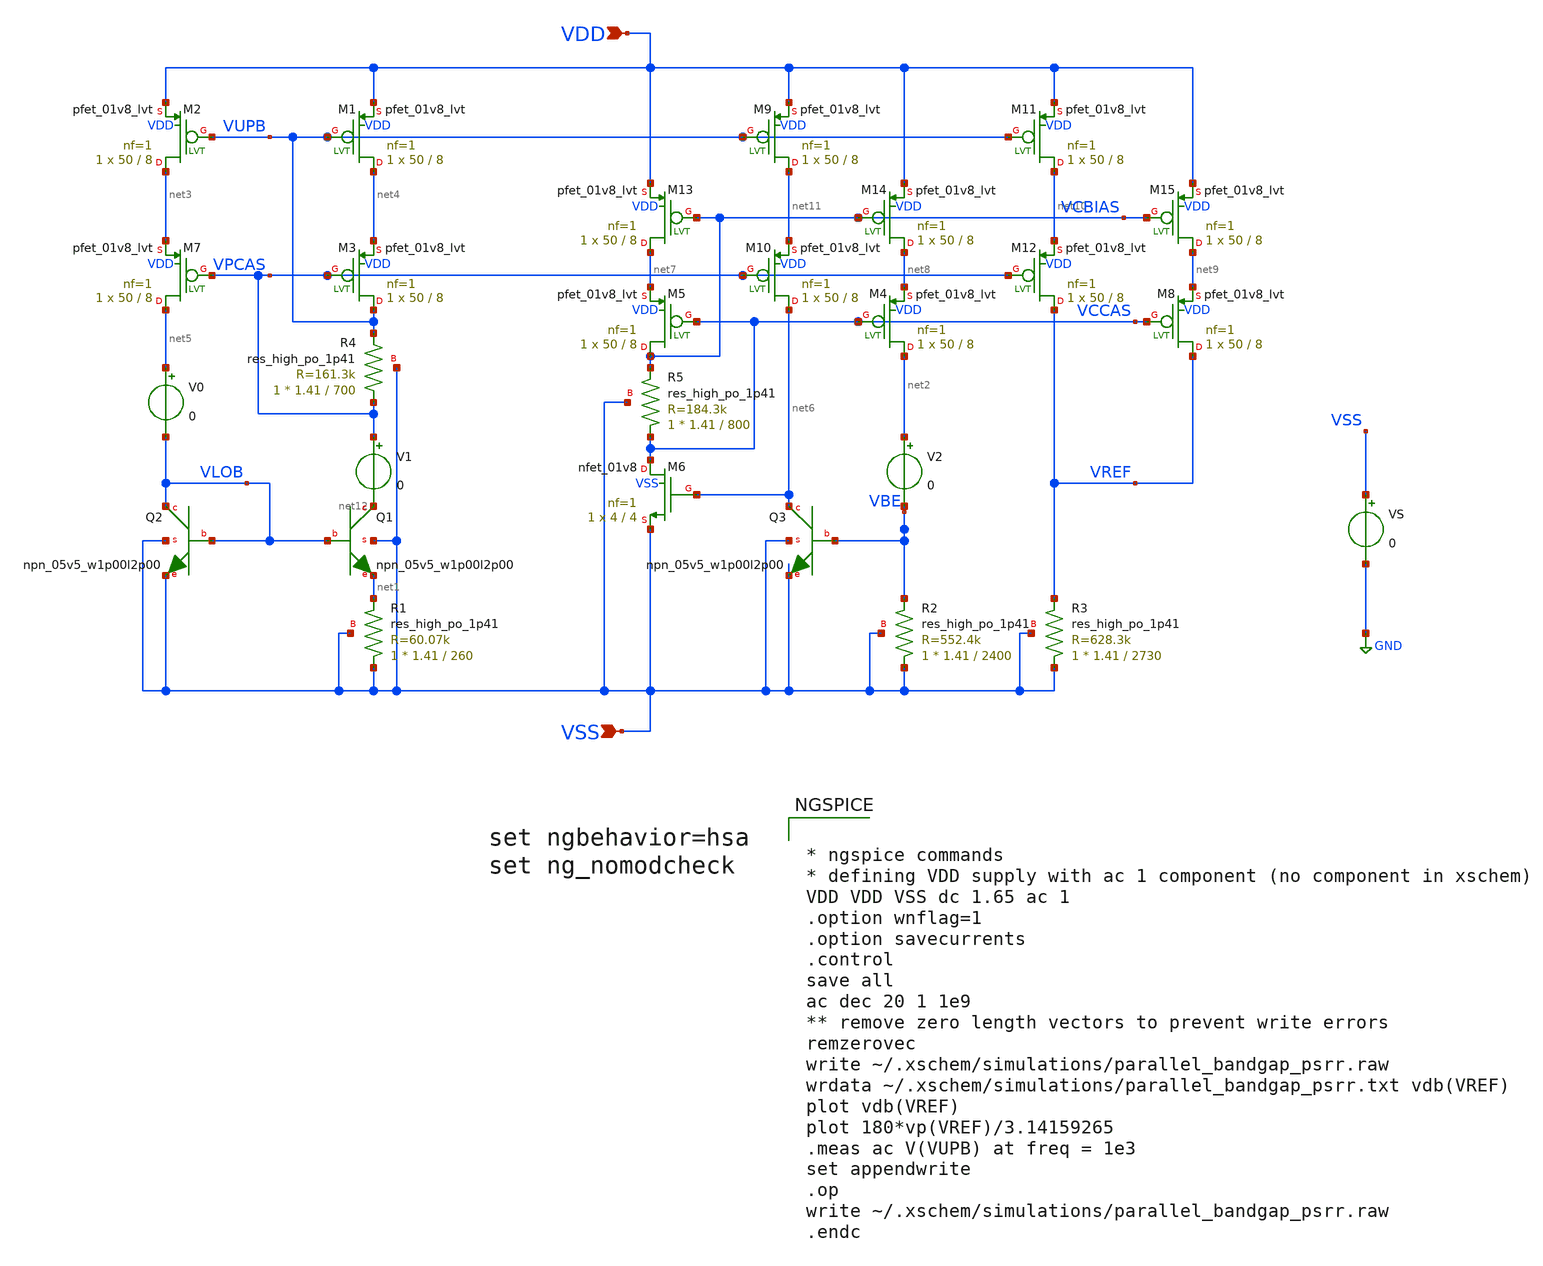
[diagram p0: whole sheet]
** sch_path: designs/parallel_bandgap_psrr.sch
**.subckt parallel_bandgap_psrr VDD VSS
*.ipin VDD
*.ipin VSS
XM1 net4 VUPB VDD VDD sky130_fd_pr__pfet_01v8_lvt L=8 W=50 nf=1 ad='int((nf+1)/2) * W/nf * 0.29' as='int((nf+2)/2) * W/nf * 0.29'
+ pd='2*int((nf+1)/2) * (W/nf + 0.29)' ps='2*int((nf+2)/2) * (W/nf + 0.29)' nrd='0.29 / W' nrs='0.29 / W'
+ sa=0 sb=0 sd=0 mult=1 m=1
XM2 net3 VUPB VDD VDD sky130_fd_pr__pfet_01v8_lvt L=8 W=50 nf=1 ad='int((nf+1)/2) * W/nf * 0.29' as='int((nf+2)/2) * W/nf * 0.29'
+ pd='2*int((nf+1)/2) * (W/nf + 0.29)' ps='2*int((nf+2)/2) * (W/nf + 0.29)' nrd='0.29 / W' nrs='0.29 / W'
+ sa=0 sb=0 sd=0 mult=1 m=1
XQ1 net12 VLOB net1 VSS sky130_fd_pr__npn_05v5_w1p00l2p00
XQ2 VLOB VLOB VSS VSS sky130_fd_pr__npn_05v5_w1p00l2p00
XR1 VSS net1 VSS sky130_fd_pr__res_high_po_1p41 L=260 mult=1 m=1
XQ3 net6 VBE VSS VSS sky130_fd_pr__npn_05v5_w1p00l2p00
XR2 VSS VBE VSS sky130_fd_pr__res_high_po_1p41 L=2400 mult=1 m=1
XM4 net2 VCCAS net8 VDD sky130_fd_pr__pfet_01v8_lvt L=8 W=50 nf=1 ad='int((nf+1)/2) * W/nf * 0.29' as='int((nf+2)/2) * W/nf * 0.29'
+ pd='2*int((nf+1)/2) * (W/nf + 0.29)' ps='2*int((nf+2)/2) * (W/nf + 0.29)' nrd='0.29 / W' nrs='0.29 / W'
+ sa=0 sb=0 sd=0 mult=1 m=1
XM5 VCBIAS VCCAS net7 VDD sky130_fd_pr__pfet_01v8_lvt L=8 W=50 nf=1 ad='int((nf+1)/2) * W/nf * 0.29'
+ as='int((nf+2)/2) * W/nf * 0.29' pd='2*int((nf+1)/2) * (W/nf + 0.29)' ps='2*int((nf+2)/2) * (W/nf + 0.29)'
+ nrd='0.29 / W' nrs='0.29 / W' sa=0 sb=0 sd=0 mult=1 m=1
XM6 VCCAS net6 VSS VSS sky130_fd_pr__nfet_01v8 L=4 W=4 nf=1 ad='int((nf+1)/2) * W/nf * 0.29' as='int((nf+2)/2) * W/nf * 0.29'
+ pd='2*int((nf+1)/2) * (W/nf + 0.29)' ps='2*int((nf+2)/2) * (W/nf + 0.29)' nrd='0.29 / W' nrs='0.29 / W'
+ sa=0 sb=0 sd=0 mult=1 m=1
XR3 VSS VREF VSS sky130_fd_pr__res_high_po_1p41 L=2730 mult=1 m=1
XM8 VREF VCCAS net9 VDD sky130_fd_pr__pfet_01v8_lvt L=8 W=50 nf=1 ad='int((nf+1)/2) * W/nf * 0.29' as='int((nf+2)/2) * W/nf * 0.29'
+ pd='2*int((nf+1)/2) * (W/nf + 0.29)' ps='2*int((nf+2)/2) * (W/nf + 0.29)' nrd='0.29 / W' nrs='0.29 / W'
+ sa=0 sb=0 sd=0 mult=1 m=1
V0 net5 VLOB 0
.save i(v0)
V2 net2 VBE 0
.save i(v2)
V1 VPCAS net12 0
.save i(v1)
XM3 VUPB VPCAS net4 VDD sky130_fd_pr__pfet_01v8_lvt L=8 W=50 nf=1 ad='int((nf+1)/2) * W/nf * 0.29' as='int((nf+2)/2) * W/nf * 0.29'
+ pd='2*int((nf+1)/2) * (W/nf + 0.29)' ps='2*int((nf+2)/2) * (W/nf + 0.29)' nrd='0.29 / W' nrs='0.29 / W'
+ sa=0 sb=0 sd=0 mult=1 m=1
XM7 net5 VPCAS net3 VDD sky130_fd_pr__pfet_01v8_lvt L=8 W=50 nf=1 ad='int((nf+1)/2) * W/nf * 0.29' as='int((nf+2)/2) * W/nf * 0.29'
+ pd='2*int((nf+1)/2) * (W/nf + 0.29)' ps='2*int((nf+2)/2) * (W/nf + 0.29)' nrd='0.29 / W' nrs='0.29 / W'
+ sa=0 sb=0 sd=0 mult=1 m=1
XR4 VPCAS VUPB VSS sky130_fd_pr__res_high_po_1p41 L=700 mult=1 m=1
XM9 net11 VUPB VDD VDD sky130_fd_pr__pfet_01v8_lvt L=8 W=50 nf=1 ad='int((nf+1)/2) * W/nf * 0.29' as='int((nf+2)/2) * W/nf * 0.29'
+ pd='2*int((nf+1)/2) * (W/nf + 0.29)' ps='2*int((nf+2)/2) * (W/nf + 0.29)' nrd='0.29 / W' nrs='0.29 / W'
+ sa=0 sb=0 sd=0 mult=1 m=1
XM10 net6 VPCAS net11 VDD sky130_fd_pr__pfet_01v8_lvt L=8 W=50 nf=1 ad='int((nf+1)/2) * W/nf * 0.29'
+ as='int((nf+2)/2) * W/nf * 0.29' pd='2*int((nf+1)/2) * (W/nf + 0.29)' ps='2*int((nf+2)/2) * (W/nf + 0.29)'
+ nrd='0.29 / W' nrs='0.29 / W' sa=0 sb=0 sd=0 mult=1 m=1
XM11 net10 VUPB VDD VDD sky130_fd_pr__pfet_01v8_lvt L=8 W=50 nf=1 ad='int((nf+1)/2) * W/nf * 0.29' as='int((nf+2)/2) * W/nf * 0.29'
+ pd='2*int((nf+1)/2) * (W/nf + 0.29)' ps='2*int((nf+2)/2) * (W/nf + 0.29)' nrd='0.29 / W' nrs='0.29 / W'
+ sa=0 sb=0 sd=0 mult=1 m=1
XM12 VREF VPCAS net10 VDD sky130_fd_pr__pfet_01v8_lvt L=8 W=50 nf=1 ad='int((nf+1)/2) * W/nf * 0.29'
+ as='int((nf+2)/2) * W/nf * 0.29' pd='2*int((nf+1)/2) * (W/nf + 0.29)' ps='2*int((nf+2)/2) * (W/nf + 0.29)'
+ nrd='0.29 / W' nrs='0.29 / W' sa=0 sb=0 sd=0 mult=1 m=1
XM13 net7 VCBIAS VDD VDD sky130_fd_pr__pfet_01v8_lvt L=8 W=50 nf=1 ad='int((nf+1)/2) * W/nf * 0.29' as='int((nf+2)/2) * W/nf * 0.29'
+ pd='2*int((nf+1)/2) * (W/nf + 0.29)' ps='2*int((nf+2)/2) * (W/nf + 0.29)' nrd='0.29 / W' nrs='0.29 / W'
+ sa=0 sb=0 sd=0 mult=1 m=1
XM14 net8 VCBIAS VDD VDD sky130_fd_pr__pfet_01v8_lvt L=8 W=50 nf=1 ad='int((nf+1)/2) * W/nf * 0.29' as='int((nf+2)/2) * W/nf * 0.29'
+ pd='2*int((nf+1)/2) * (W/nf + 0.29)' ps='2*int((nf+2)/2) * (W/nf + 0.29)' nrd='0.29 / W' nrs='0.29 / W'
+ sa=0 sb=0 sd=0 mult=1 m=1
XR5 VCCAS VCBIAS VSS sky130_fd_pr__res_high_po_1p41 L=800 mult=1 m=1
XM15 net9 VCBIAS VDD VDD sky130_fd_pr__pfet_01v8_lvt L=8 W=50 nf=1 ad='int((nf+1)/2) * W/nf * 0.29' as='int((nf+2)/2) * W/nf * 0.29'
+ pd='2*int((nf+1)/2) * (W/nf + 0.29)' ps='2*int((nf+2)/2) * (W/nf + 0.29)' nrd='0.29 / W' nrs='0.29 / W'
+ sa=0 sb=0 sd=0 mult=1 m=1
VS VSS GND 0
**** begin user architecture code


* ngspice commands
* defining VDD supply with ac 1 component (no component in xschem)
VDD VDD VSS dc 1.65 ac 1
.option wnflag=1
.option savecurrents
.control
save all
ac dec 20 1 1e9
** remove zero length vectors to prevent write errors
remzerovec
write ~/.xschem/simulations/parallel_bandgap_psrr.raw
wrdata ~/.xschem/simulations/parallel_bandgap_psrr.txt vdb(VREF)
plot vdb(VREF)
plot 180*vp(VREF)/3.14159265
.meas ac V(VUPB) at freq = 1e3
set appendwrite
.op
write ~/.xschem/simulations/parallel_bandgap_psrr.raw
.endc



** opencircuitdesign pdks install
.lib /foss/pdks/sky130A/libs.tech/ngspice/sky130.lib.corners.spice tt

**** end user architecture code
**.ends
.GLOBAL GND
.end
